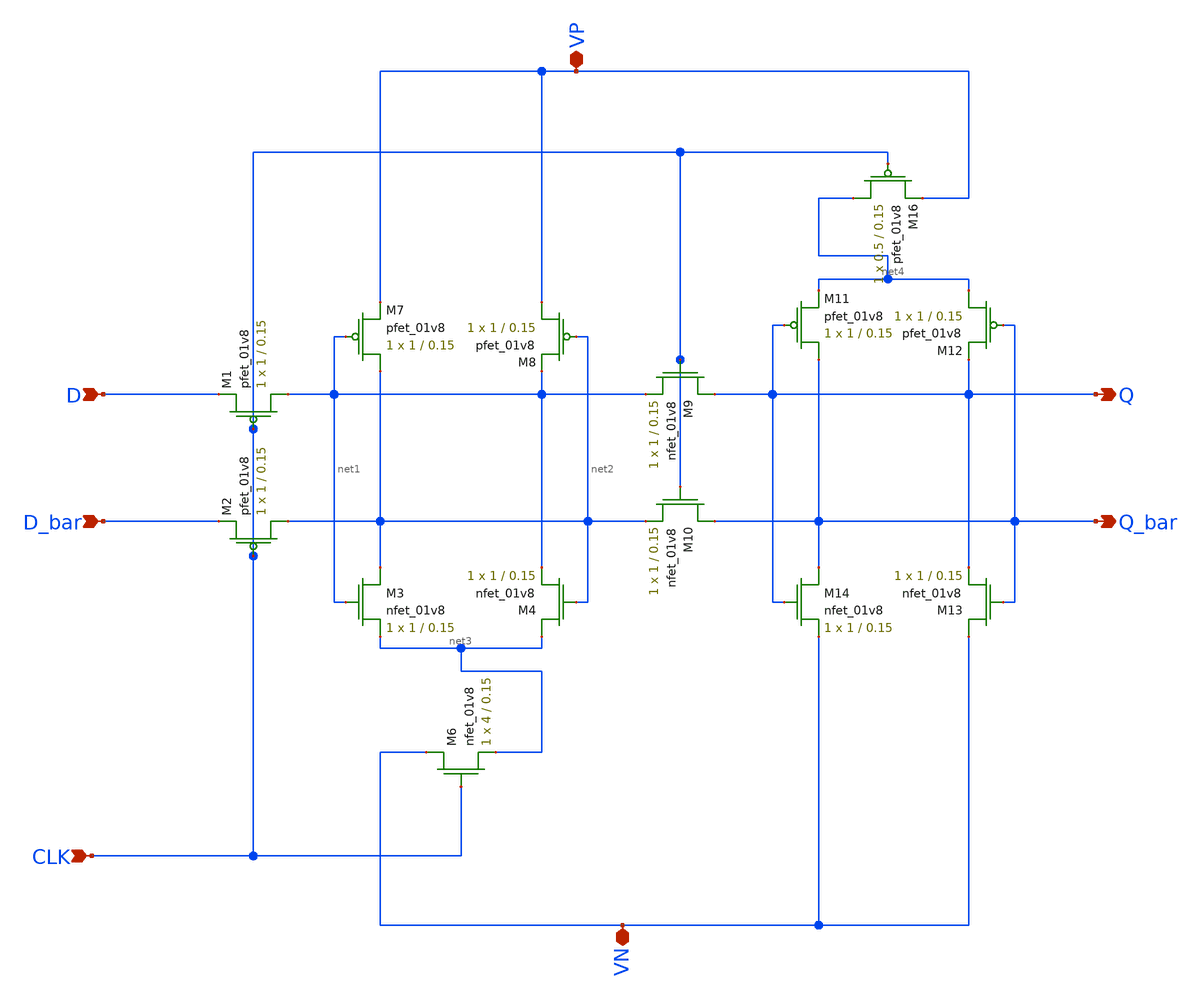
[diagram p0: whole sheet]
** sch_path: mp2/schematic/csrl_latch_final.sch
**.subckt csrl_latch_final VP VN CLK Q Q_bar D D_bar
*.iopin VP
*.iopin VN
*.ipin CLK
*.opin Q
*.opin Q_bar
*.ipin D
*.ipin D_bar
XM7 net2 net1 VP VDD sky130_fd_pr__pfet_01v8 L=0.15 W=1 nf=1 ad='int((nf+1)/2) * W/nf * 0.29' as='int((nf+2)/2) * W/nf * 0.29'
+ pd='2*int((nf+1)/2) * (W/nf + 0.29)' ps='2*int((nf+2)/2) * (W/nf + 0.29)' nrd='0.29 / W' nrs='0.29 / W'
+ sa=0 sb=0 sd=0 mult=1 m=1
XM8 VP net2 net1 VDD sky130_fd_pr__pfet_01v8 L=0.15 W=1 nf=1 ad='int((nf+1)/2) * W/nf * 0.29' as='int((nf+2)/2) * W/nf * 0.29'
+ pd='2*int((nf+1)/2) * (W/nf + 0.29)' ps='2*int((nf+2)/2) * (W/nf + 0.29)' nrd='0.29 / W' nrs='0.29 / W'
+ sa=0 sb=0 sd=0 mult=1 m=1
XM3 net2 net1 net3 GND sky130_fd_pr__nfet_01v8 L=0.15 W=1 nf=1 ad='int((nf+1)/2) * W/nf * 0.29' as='int((nf+2)/2) * W/nf * 0.29'
+ pd='2*int((nf+1)/2) * (W/nf + 0.29)' ps='2*int((nf+2)/2) * (W/nf + 0.29)' nrd='0.29 / W' nrs='0.29 / W'
+ sa=0 sb=0 sd=0 mult=1 m=1
XM4 net3 net2 net1 GND sky130_fd_pr__nfet_01v8 L=0.15 W=1 nf=1 ad='int((nf+1)/2) * W/nf * 0.29' as='int((nf+2)/2) * W/nf * 0.29'
+ pd='2*int((nf+1)/2) * (W/nf + 0.29)' ps='2*int((nf+2)/2) * (W/nf + 0.29)' nrd='0.29 / W' nrs='0.29 / W'
+ sa=0 sb=0 sd=0 mult=1 m=1
XM6 VN CLK net3 GND sky130_fd_pr__nfet_01v8 L=0.15 W=4 nf=1 ad='int((nf+1)/2) * W/nf * 0.29' as='int((nf+2)/2) * W/nf * 0.29'
+ pd='2*int((nf+1)/2) * (W/nf + 0.29)' ps='2*int((nf+2)/2) * (W/nf + 0.29)' nrd='0.29 / W' nrs='0.29 / W'
+ sa=0 sb=0 sd=0 mult=1 m=1
XM9 Q CLK net1 GND sky130_fd_pr__nfet_01v8 L=0.15 W=1 nf=1 ad='int((nf+1)/2) * W/nf * 0.29' as='int((nf+2)/2) * W/nf * 0.29'
+ pd='2*int((nf+1)/2) * (W/nf + 0.29)' ps='2*int((nf+2)/2) * (W/nf + 0.29)' nrd='0.29 / W' nrs='0.29 / W'
+ sa=0 sb=0 sd=0 mult=1 m=1
XM10 Q_bar CLK net2 GND sky130_fd_pr__nfet_01v8 L=0.15 W=1 nf=1 ad='int((nf+1)/2) * W/nf * 0.29' as='int((nf+2)/2) * W/nf * 0.29'
+ pd='2*int((nf+1)/2) * (W/nf + 0.29)' ps='2*int((nf+2)/2) * (W/nf + 0.29)' nrd='0.29 / W' nrs='0.29 / W'
+ sa=0 sb=0 sd=0 mult=1 m=1
XM11 Q_bar Q net4 VDD sky130_fd_pr__pfet_01v8 L=0.15 W=1 nf=1 ad='int((nf+1)/2) * W/nf * 0.29' as='int((nf+2)/2) * W/nf * 0.29'
+ pd='2*int((nf+1)/2) * (W/nf + 0.29)' ps='2*int((nf+2)/2) * (W/nf + 0.29)' nrd='0.29 / W' nrs='0.29 / W'
+ sa=0 sb=0 sd=0 mult=1 m=1
XM12 net4 Q_bar Q VDD sky130_fd_pr__pfet_01v8 L=0.15 W=1 nf=1 ad='int((nf+1)/2) * W/nf * 0.29' as='int((nf+2)/2) * W/nf * 0.29'
+ pd='2*int((nf+1)/2) * (W/nf + 0.29)' ps='2*int((nf+2)/2) * (W/nf + 0.29)' nrd='0.29 / W' nrs='0.29 / W'
+ sa=0 sb=0 sd=0 mult=1 m=1
XM13 VN Q_bar Q GND sky130_fd_pr__nfet_01v8 L=0.15 W=1 nf=1 ad='int((nf+1)/2) * W/nf * 0.29' as='int((nf+2)/2) * W/nf * 0.29'
+ pd='2*int((nf+1)/2) * (W/nf + 0.29)' ps='2*int((nf+2)/2) * (W/nf + 0.29)' nrd='0.29 / W' nrs='0.29 / W'
+ sa=0 sb=0 sd=0 mult=1 m=1
XM14 Q_bar Q VN GND sky130_fd_pr__nfet_01v8 L=0.15 W=1 nf=1 ad='int((nf+1)/2) * W/nf * 0.29' as='int((nf+2)/2) * W/nf * 0.29'
+ pd='2*int((nf+1)/2) * (W/nf + 0.29)' ps='2*int((nf+2)/2) * (W/nf + 0.29)' nrd='0.29 / W' nrs='0.29 / W'
+ sa=0 sb=0 sd=0 mult=1 m=1
XM16 net4 CLK VP VDD sky130_fd_pr__pfet_01v8 L=0.15 W=0.5 nf=1 ad='int((nf+1)/2) * W/nf * 0.29' as='int((nf+2)/2) * W/nf * 0.29'
+ pd='2*int((nf+1)/2) * (W/nf + 0.29)' ps='2*int((nf+2)/2) * (W/nf + 0.29)' nrd='0.29 / W' nrs='0.29 / W'
+ sa=0 sb=0 sd=0 mult=1 m=1
XM1 net1 CLK D VDD sky130_fd_pr__pfet_01v8 L=0.15 W=1 nf=1 ad='int((nf+1)/2) * W/nf * 0.29' as='int((nf+2)/2) * W/nf * 0.29'
+ pd='2*int((nf+1)/2) * (W/nf + 0.29)' ps='2*int((nf+2)/2) * (W/nf + 0.29)' nrd='0.29 / W' nrs='0.29 / W'
+ sa=0 sb=0 sd=0 mult=1 m=1
XM2 net2 CLK D_bar VDD sky130_fd_pr__pfet_01v8 L=0.15 W=1 nf=1 ad='int((nf+1)/2) * W/nf * 0.29' as='int((nf+2)/2) * W/nf * 0.29'
+ pd='2*int((nf+1)/2) * (W/nf + 0.29)' ps='2*int((nf+2)/2) * (W/nf + 0.29)' nrd='0.29 / W' nrs='0.29 / W'
+ sa=0 sb=0 sd=0 mult=1 m=1
**.ends
.end
